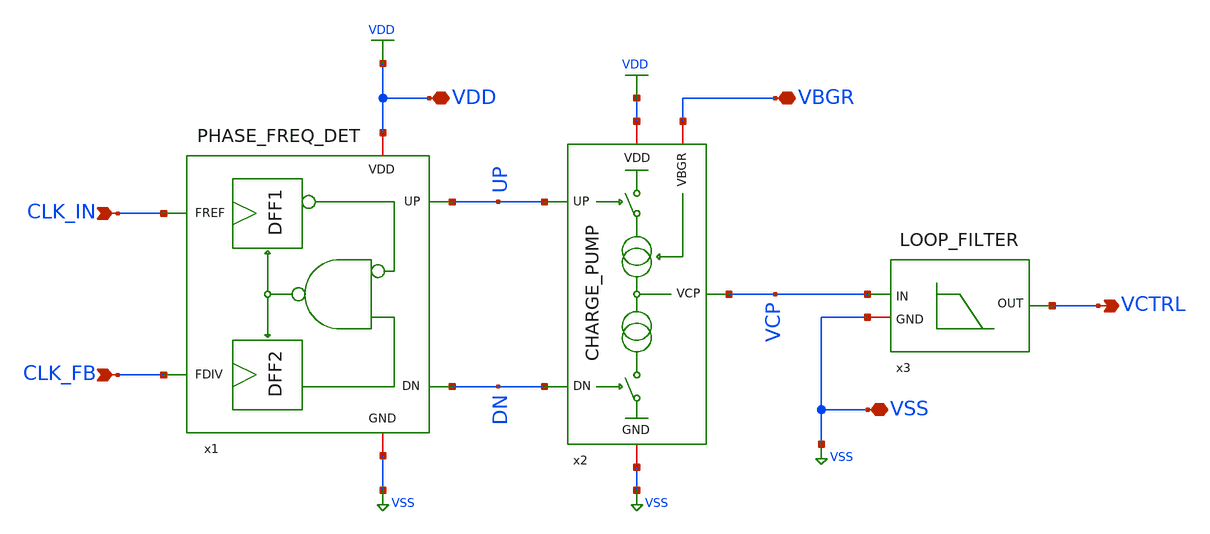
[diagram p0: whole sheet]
** sch_path: xschem/PFD_CP_LF.sch
**.subckt PFD_CP_LF CLK_IN VCTRL VDD VSS CLK_FB VBGR
*.ipin CLK_IN
*.opin VCTRL
*.iopin VDD
*.iopin VSS
*.ipin CLK_FB
*.iopin VBGR
x1 CLK_IN UP VDD VSS CLK_FB DN PHASE_FREQ_DET
x2 UP VDD VCP VBGR VSS DN CHARGE_PUMP
x3 VCTRL VCP VSS LOOP_FILTER
**.ends

* expanding   symbol:  xschem/PHASE_FREQ_DET.sym # of pins=6
** sym_path: xschem/PHASE_FREQ_DET.sym
** sch_path: xschem/PHASE_FREQ_DET.sch
.subckt PHASE_FREQ_DET FREF UP VDD GND FDIV DN
*.opin UP
*.ipin FREF
*.iopin VDD
*.iopin GND
*.opin DN
*.ipin FDIV
* noconn #net2
x1 net1 UP FREF VDD nRST VDD GND sg13g2_dfrbp_2
x2 DN net2 FDIV VDD nRST VDD GND sg13g2_dfrbp_2
x3 nRST net1 DN VDD GND sg13g2_nand2_2
.ends


* expanding   symbol:  xschem/CHARGE_PUMP.sym # of pins=6
** sym_path: xschem/CHARGE_PUMP.sym
** sch_path: xschem/CHARGE_PUMP.sch
.subckt CHARGE_PUMP UP VDD VCP VBGR GND DN
*.opin VCP
*.ipin UP
*.ipin DN
*.iopin GND
*.iopin VBGR
*.iopin VDD
XM2 Vbn Vbn net5 bulk2 sg13_lv_nmos w=40.7u l=2u ng=5 m=1 mm_ok=1
XM8 net2 GND VDD bulk1 sg13_lv_pmos w=29.6u l=2u ng=5 m=1 mm_ok=1
XM11 Vbp Vbp net2 bulk1 sg13_lv_pmos w=163.6u l=2u ng=20 m=1 mm_ok=1
XM3 Vbn Vbp net1 bulk1 sg13_lv_pmos w=163.6u l=2u ng=20 m=1 mm_ok=1
XM4 net1 GND VDD bulk1 sg13_lv_pmos w=29.6u l=2u ng=5 m=1 mm_ok=1
XM7 net3 UP VDD bulk1 sg13_lv_pmos w=29.6u l=2u ng=5 m=1 mm_ok=1
XM9 VCP Vbp net3 bulk1 sg13_lv_pmos w=163.6u l=2u ng=20 m=1 mm_ok=1
XM10 net5 VDD GND bulk2 sg13_lv_nmos w=6u l=2u ng=1 m=1 mm_ok=1
XM1 net4 DN GND bulk2 sg13_lv_nmos w=6u l=2u ng=1 m=1 mm_ok=1
XM5 VCP Vbn net4 bulk2 sg13_lv_nmos w=40.7u l=2u ng=5 m=1 mm_ok=1
XM6 Vbp VBGR GND bulk2 sg13_lv_nmos w=3.9u l=2u ng=1 m=1 mm_ok=1
XR1 VDD bulk1 ntap1 R=1.319 w=51e-6 l=36e-6 rw=0.3e-6
XR2 VDD bulk1 ntap1 R=2.51 w=30.5e-6 l=15.5e-6 rw=0.3e-6
XR3 GND bulk2 ptap1 R=9.234 w=5.68e-6 l=7.26e-6 rw=0.3e-6
XR4 GND bulk2 ptap1 R=2.717 w=30e-6 l=12.54e-6 rw=0.3e-6
XR5 GND bulk2 ptap1 R=4.486 w=20e-6 l=6e-6 rw=0.3e-6
.ends


* expanding   symbol:  xschem/LOOP_FILTER.sym # of pins=3
** sym_path: xschem/LOOP_FILTER.sym
** sch_path: xschem/LOOP_FILTER.sch
.subckt LOOP_FILTER OUT IN GND
*.opin OUT
*.iopin GND
*.ipin IN
XC2 OUT GND cap_cmim w=18.63e-6 l=18.63e-6 m=4 mm_ok=1
XC1 net1 GND cap_cmim w=48.34e-6 l=48.34e-6 m=16 mm_ok=1
XR2 OUT IN sub! rppd w=2e-6 l=407.2e-6 m=1 b=0 mm_ok=1
XR1 net1 IN sub! rppd w=2e-6 l=407.2e-6 m=1 b=0 mm_ok=1
XR3 GND sub! ptap1 R=1.462 w=46.34e-6 l=32.18e-6 rw=0.3e-6
XR4 GND sub! ptap1 R=1.462 w=46.34e-6 l=32.18e-6 rw=0.3e-6
.ends


* expanding   symbol:  sg13g2_stdcells/sg13g2_dfrbp_2.sym # of pins=5
** sym_path: sg13g2_stdcells/sg13g2_dfrbp_2.sym
** sch_path: sg13g2_stdcells/sg13g2_dfrbp_2.sch
.subckt sg13g2_dfrbp_2 Q Q_N CLK D RESET_B VDD VSS
*.ipin D
*.ipin RESET_B
*.ipin CLK
*.opin Q
*.opin Q_N
*.iopin VDD
*.iopin VSS
XM1 Db D net12 VSS sg13_lv_nmos w=420.00n l=130.00n ng=1 m=1 mm_ok=1
XM2 net12 RESET_B VSS VSS sg13_lv_nmos w=420.00n l=130.00n ng=1 m=1 mm_ok=1
XM3 net2 clkneg net11 VSS sg13_lv_nmos w=420.00n l=130.00n ng=1 m=1 mm_ok=1
XM4 net11 net3 VSS VSS sg13_lv_nmos w=420.00n l=130.00n ng=1 m=1 mm_ok=1
XM5 net3 net2 net7 VSS sg13_lv_nmos w=420.00n l=130.00n ng=1 m=1 mm_ok=1
XM6 net7 RESET_B VSS VSS sg13_lv_nmos w=420.00n l=130.00n ng=1 m=1 mm_ok=1
XM7 Q_N net2 VSS VSS sg13_lv_nmos w=1.48u l=130.00n ng=2 m=1 mm_ok=1
XM8 net1 net2 VSS VSS sg13_lv_nmos w=640.00n l=130.00n ng=1 m=1 mm_ok=1
XM9 Q net1 VSS VSS sg13_lv_nmos w=1.48u l=130.00n ng=2 m=1 mm_ok=1
XM10 clkneg CLK VSS VSS sg13_lv_nmos w=740.00n l=130.00n ng=1 m=1 mm_ok=1
XM11 clkpos clkneg VSS VSS sg13_lv_nmos w=740.00n l=130.00n ng=1 m=1 mm_ok=1
XM12 Db clkneg net4 VSS sg13_lv_nmos w=420.00n l=130.00n ng=1 m=1 mm_ok=1
XM13 net4 clkpos net10 VSS sg13_lv_nmos w=420.00n l=130.00n ng=1 m=1 mm_ok=1
XM14 net10 net5 net6 VSS sg13_lv_nmos w=420.00n l=130.00n ng=1 m=1 mm_ok=1
XM15 net6 RESET_B VSS VSS sg13_lv_nmos w=420.00n l=130.00n ng=1 m=1 mm_ok=1
XM16 net5 net4 VSS VSS sg13_lv_nmos w=740.00n l=130.00n ng=1 m=1 mm_ok=1
XM17 net5 clkpos net2 VSS sg13_lv_nmos w=740.00n l=130.00n ng=1 m=1 mm_ok=1
XM18 Db RESET_B VDD VDD sg13_lv_pmos w=420.00n l=130.00n ng=1 m=1 mm_ok=1
XM19 Db D VDD VDD sg13_lv_pmos w=420.00n l=130.00n ng=1 m=1 mm_ok=1
XM20 net9 net3 VDD VDD sg13_lv_pmos w=420.00n l=130.00n ng=1 m=1 mm_ok=1
XM21 net2 clkpos net9 VDD sg13_lv_pmos w=420.00n l=130.00n ng=1 m=1 mm_ok=1
XM22 net3 net2 VDD VDD sg13_lv_pmos w=420.00n l=130.00n ng=1 m=1 mm_ok=1
XM23 net3 RESET_B VDD VDD sg13_lv_pmos w=420.00n l=130.00n ng=1 m=1 mm_ok=1
XM24 Q_N net2 VDD VDD sg13_lv_pmos w=2.24u l=130.00n ng=2 m=1 mm_ok=1
XM25 net1 net2 VDD VDD sg13_lv_pmos w=1.000u l=130.00n ng=1 m=1 mm_ok=1
XM26 Q net1 VDD VDD sg13_lv_pmos w=2.24u l=130.00n ng=2 m=1 mm_ok=1
XM27 clkneg CLK VDD VDD sg13_lv_pmos w=1.12u l=130.00n ng=1 m=1 mm_ok=1
XM28 clkpos clkneg VDD VDD sg13_lv_pmos w=1.12u l=130.00n ng=1 m=1 mm_ok=1
XM29 Db clkpos net4 VDD sg13_lv_pmos w=420.00n l=130.00n ng=1 m=1 mm_ok=1
XM30 net8 net5 VDD VDD sg13_lv_pmos w=420.00n l=130.00n ng=1 m=1 mm_ok=1
XM31 net4 clkneg net8 VDD sg13_lv_pmos w=420.00n l=130.00n ng=1 m=1 mm_ok=1
XM32 net4 RESET_B VDD VDD sg13_lv_pmos w=420.00n l=130.00n ng=1 m=1 mm_ok=1
XM33 net5 net4 VDD VDD sg13_lv_pmos w=1.000u l=130.00n ng=1 m=1 mm_ok=1
XM34 net5 clkneg net2 VDD sg13_lv_pmos w=1.000u l=130.00n ng=1 m=1 mm_ok=1
.ends


* expanding   symbol:  sg13g2_stdcells/sg13g2_nand2_2.sym # of pins=3
** sym_path: sg13g2_stdcells/sg13g2_nand2_2.sym
** sch_path: sg13g2_stdcells/sg13g2_nand2_2.sch
.subckt sg13g2_nand2_2 Y A B VDD VSS
*.iopin VDD
*.iopin VSS
*.opin Y
*.ipin B
*.ipin A
XM1 Y A net1 VSS sg13_lv_nmos w=1.44u l=130.00n ng=2 m=1 mm_ok=1
XM2 net1 B VSS VSS sg13_lv_nmos w=1.44u l=130.00n ng=2 m=1 mm_ok=1
XM3 Y A VDD VDD sg13_lv_pmos w=2.24u l=130.00n ng=2 m=1 mm_ok=1
XM4 Y B VDD VDD sg13_lv_pmos w=2.24u l=130.00n ng=2 m=1 mm_ok=1
.ends

.GLOBAL VSS
.GLOBAL VDD
.GLOBAL GND
.end
